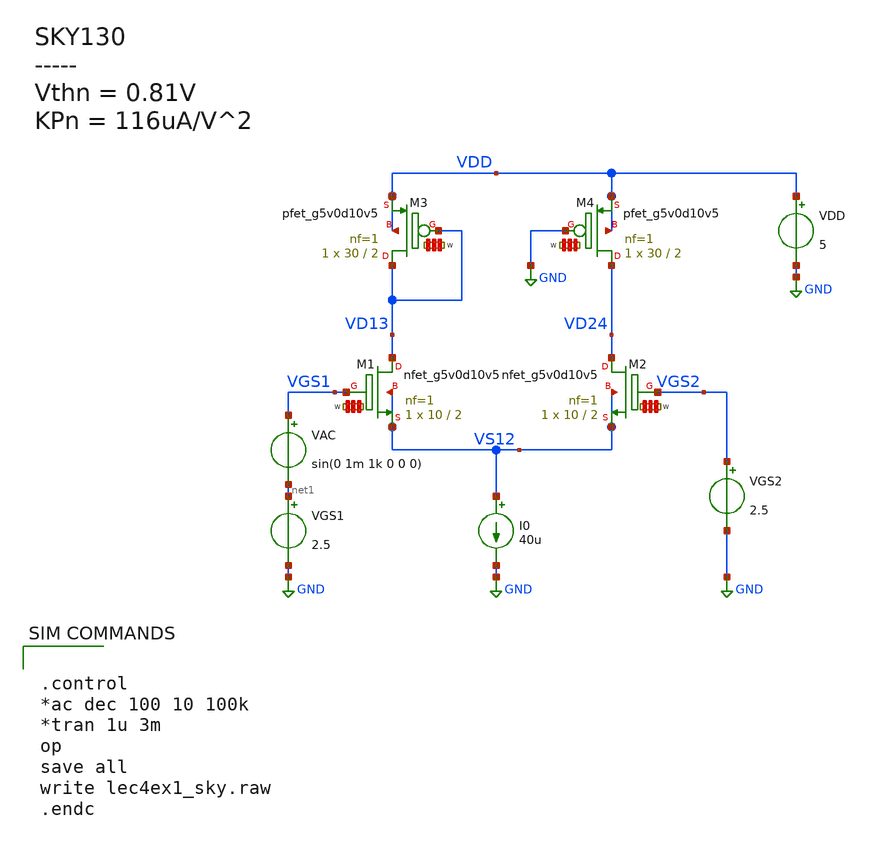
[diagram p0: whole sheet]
** sch_path: lec4ex1_sky.sch
**.subckt lec4ex1_sky
XM1 VD13 VGS1 VS12 VS12 sky130_fd_pr__nfet_g5v0d10v5 L=2 W='10 * 1 ' nf=1 ad='int((nf+1)/2) * W / nf * 0.29'
+ as='int((nf+2)/2) * W / nf * 0.29' pd='2*int((nf+1)/2) * (W / nf + 0.29)' ps='2*int((nf+2)/2) * (W / nf + 0.29)'
+ nrd='0.29 / W ' nrs='0.29 / W ' sa=0 sb=0 sd=0 mult=1 m=1
XM2 VD24 VGS2 VS12 VS12 sky130_fd_pr__nfet_g5v0d10v5 L=2 W='10 * 1 ' nf=1 ad='int((nf+1)/2) * W / nf * 0.29'
+ as='int((nf+2)/2) * W / nf * 0.29' pd='2*int((nf+1)/2) * (W / nf + 0.29)' ps='2*int((nf+2)/2) * (W / nf + 0.29)'
+ nrd='0.29 / W ' nrs='0.29 / W ' sa=0 sb=0 sd=0 mult=1 m=1
VGS1 net1 GND 2.5
I0 VS12 GND 40u
VAC VGS1 net1 sin(0 1m 1k 0 0 0)
VGS2 VGS2 GND 2.5
XM3 VD13 VD13 VDD VDD sky130_fd_pr__pfet_g5v0d10v5 L=2 W='30 * 1 ' nf=1 ad='int((nf+1)/2) * W / nf * 0.29'
+ as='int((nf+2)/2) * W / nf * 0.29' pd='2*int((nf+1)/2) * (W / nf + 0.29)' ps='2*int((nf+2)/2) * (W / nf + 0.29)'
+ nrd='0.29 / W ' nrs='0.29 / W ' sa=0 sb=0 sd=0 mult=1 m=1
XM4 VD24 GND VDD VDD sky130_fd_pr__pfet_g5v0d10v5 L=2 W='30 * 1 ' nf=1 ad='int((nf+1)/2) * W / nf * 0.29'
+ as='int((nf+2)/2) * W / nf * 0.29' pd='2*int((nf+1)/2) * (W / nf + 0.29)' ps='2*int((nf+2)/2) * (W / nf + 0.29)'
+ nrd='0.29 / W ' nrs='0.29 / W ' sa=0 sb=0 sd=0 mult=1 m=1
VDD VDD GND 5
**** begin user architecture code


.control
*ac dec 100 10 100k
*tran 1u 3m
op
save all
write lec4ex1_sky.raw
.endc



** opencircuitdesign pdks install
.lib $::SKYWATER_MODELS/sky130.lib.spice tt


**** end user architecture code
**.ends
.GLOBAL GND
.end
